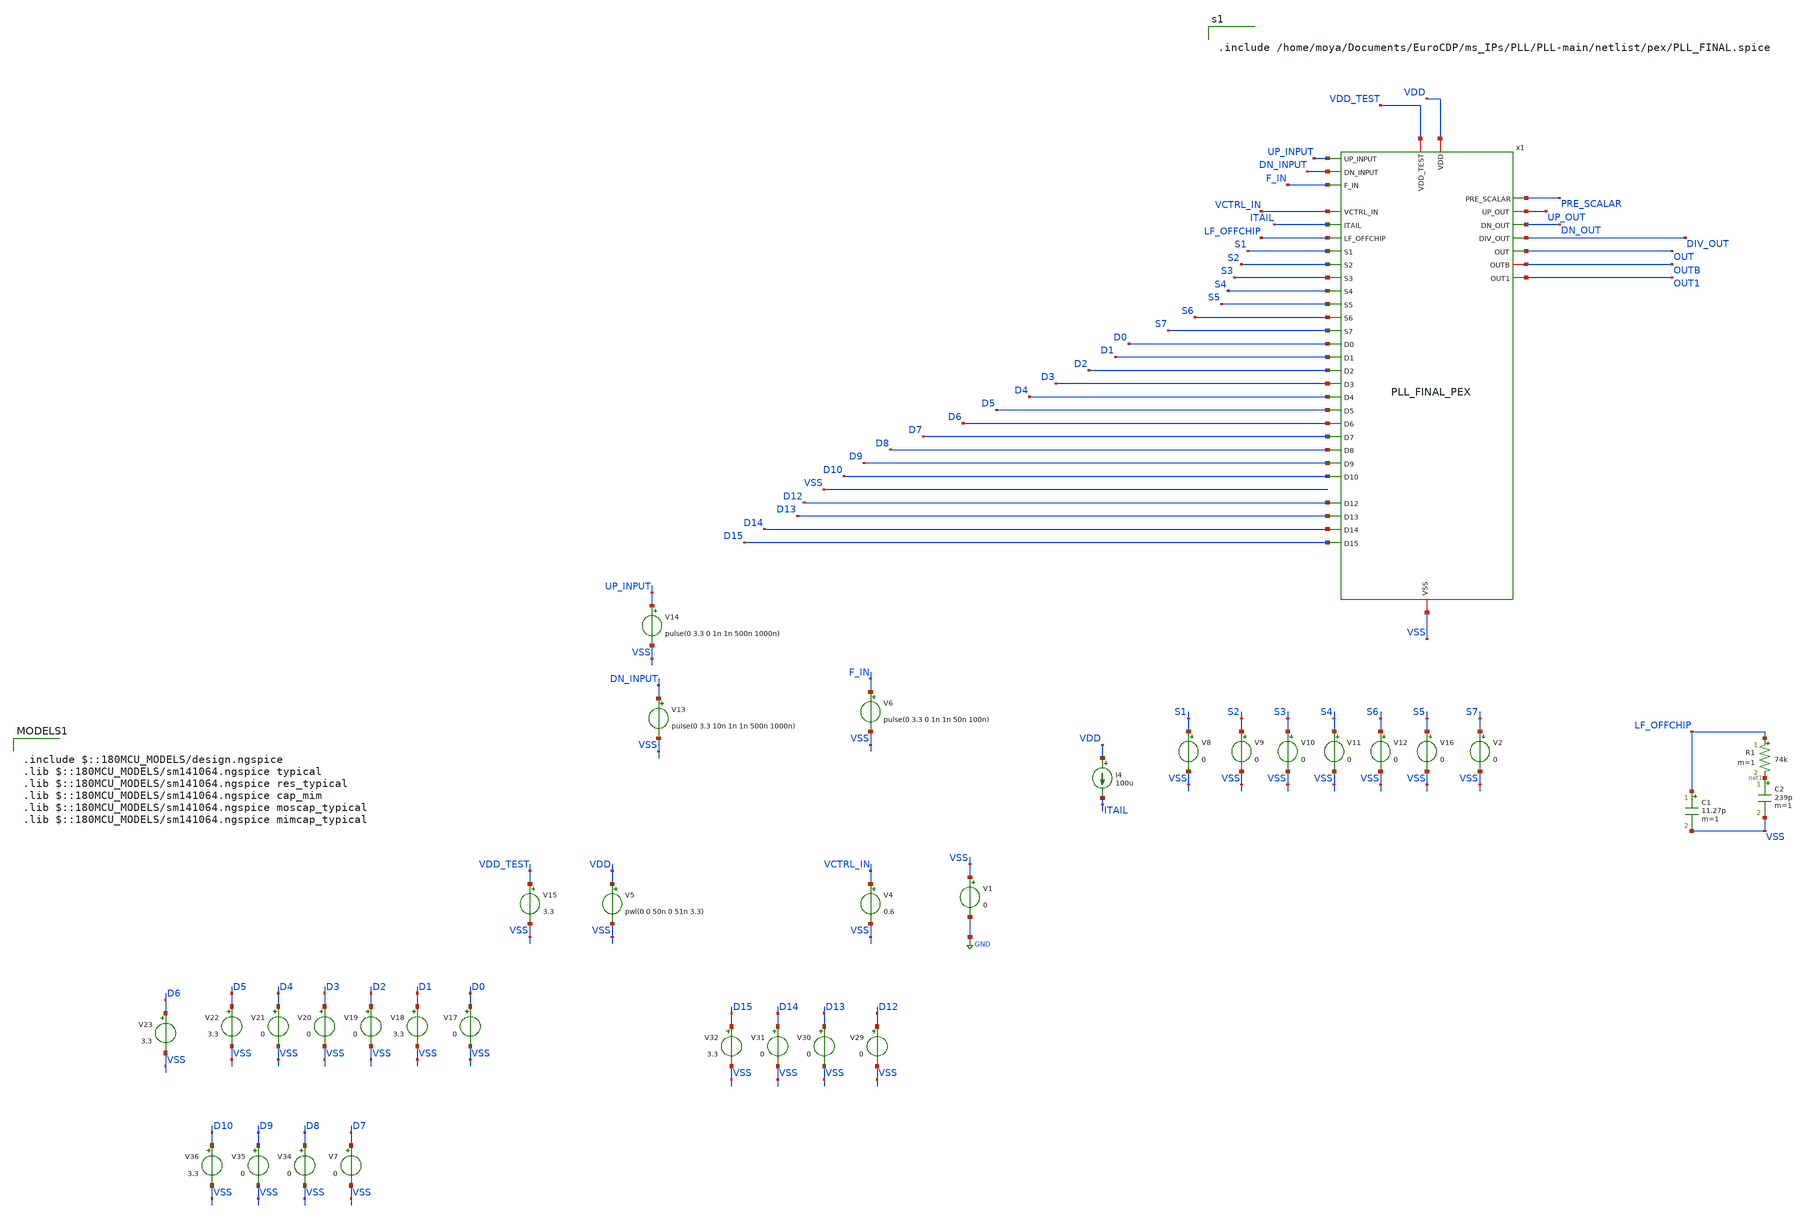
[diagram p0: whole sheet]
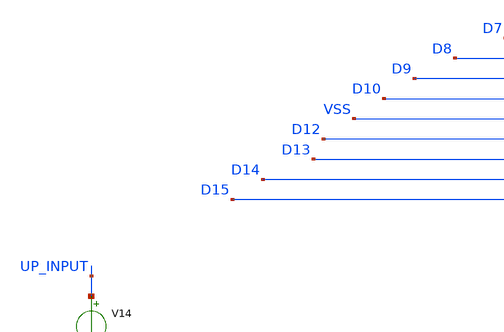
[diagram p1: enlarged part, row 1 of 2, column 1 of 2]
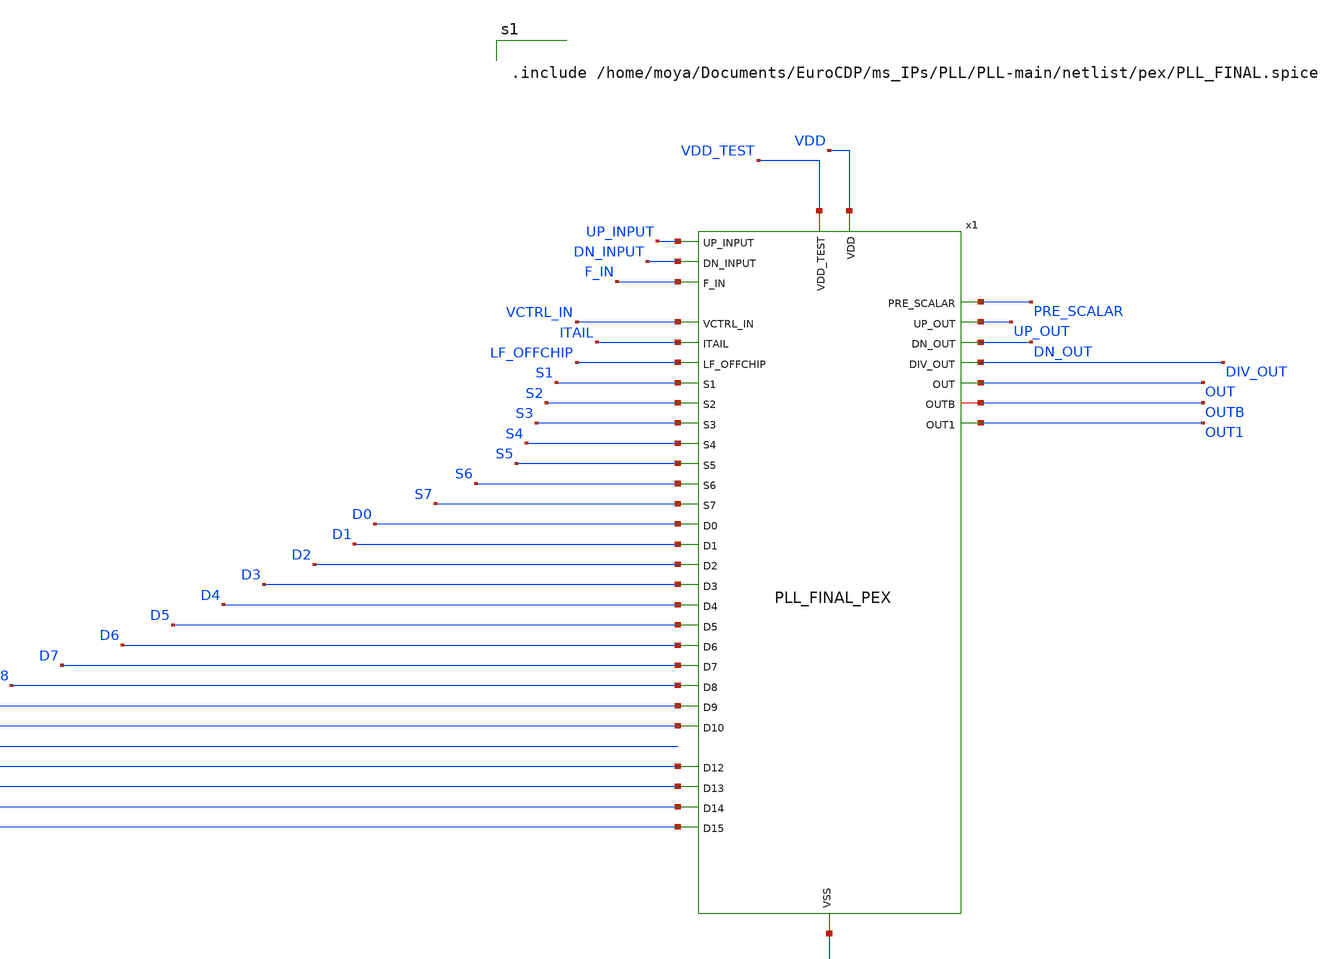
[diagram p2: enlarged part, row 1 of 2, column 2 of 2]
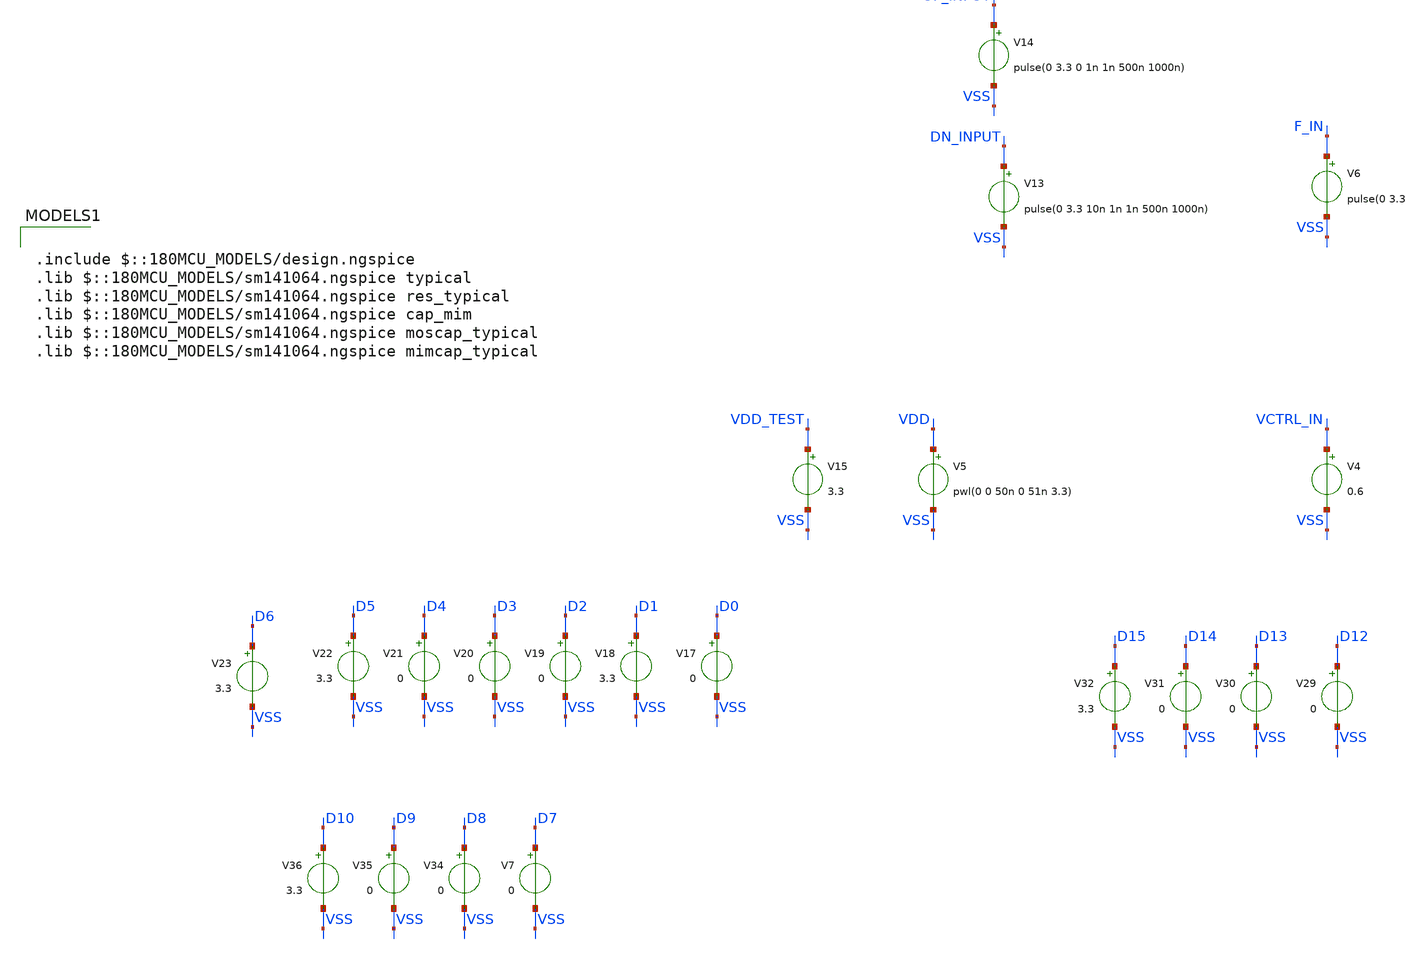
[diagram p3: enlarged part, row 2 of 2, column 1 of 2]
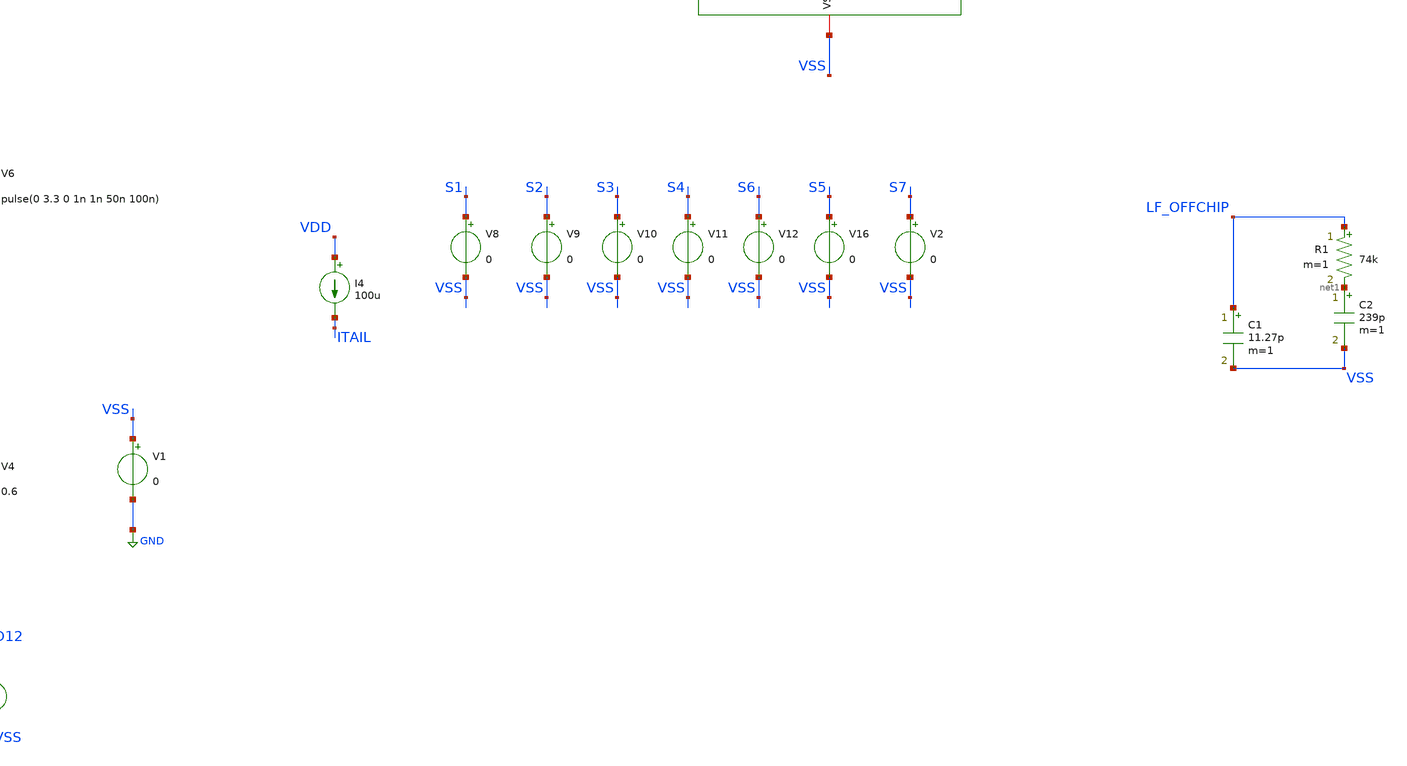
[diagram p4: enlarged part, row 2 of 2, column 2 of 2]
** sch_path: PLL-main/testbench/tran/xschem/TB_PLL_TOP_pex.sch
**.subckt TB_PLL_TOP_pex
V1 VSS GND 0
V4 VCTRL_IN VSS 0.6
V6 F_IN VSS pulse(0 3.3 0 1n 1n 50n 100n)
I4 VDD ITAIL 100u
V8 S1 VSS 0
V9 S2 VSS 0
V10 S3 VSS 0
V11 S4 VSS 0
V12 S6 VSS 0
V13 DN_INPUT VSS pulse(0 3.3 10n 1n 1n 500n 1000n)
V14 UP_INPUT VSS pulse(0 3.3 0 1n 1n 500n 1000n)
V15 VDD_TEST VSS 3.3
C1 LF_OFFCHIP VSS 11.27p m=1
R1 LF_OFFCHIP net1 74k m=1
C2 net1 VSS 239p m=1
V16 S5 VSS 0
V17 D0 VSS 0
V18 D1 VSS 3.3
V19 D2 VSS 0
V20 D3 VSS 0
V21 D4 VSS 0
V22 D5 VSS 3.3
V23 D6 VSS 3.3
V29 D12 VSS 0
V30 D13 VSS 0
V31 D14 VSS 0
V32 D15 VSS 3.3
V2 S7 VSS 0
V5 VDD VSS pwl(0 0 50n 0 51n 3.3)
V7 D7 VSS 0
V34 D8 VSS 0
V35 D9 VSS 0
V36 D10 VSS 3.3
x1 VDD_TEST D12 D0 UP_INPUT D13 D1 DN_INPUT VSS D14 D2 PRE_SCALAR UP_OUT D15 D3 F_IN DN_OUT D4 ITAIL
+ DIV_OUT D5 S1 S6 D6 VCTRL_IN D7 S2 D8 S3 OUT D9 OUTB S4 LF_OFFCHIP D10 S5 S7 OUT1 VDD PLL_FINAL
**** begin user architecture code


*.include pex_A_MUX.spice
*.include pex_VCO_DFF_C.spice
*.include Tappered-Buffer_1_pex.spice
*.include pex_PFD_T2.spice
*.include pex_CP.spice
*.include Res_74k_pex.spice
*.include pex_cap_11p.spice
*.include pex_cap_240p.spice
*.include pex_PLL_TOP_MUX_8.spice
*.include pex_7b_divider_magic.spice
*.include pex_PLL_TOP_MUX_2.spice
*.include Tappered-Buffer_1_pex.spice
*.option RSHUNT=1e18
**.option ABSTOL=1e-12
**.option VNTOL=1e-12
**.option CHGTOL=1e-14
.option RELTOL=1e-3
.option gmin=1e-12
**.option trtol=1
**.OPTION ITL4=500
.control
*save x1.vco_dff_c_0.vctrl.t19
*+ x1.pre_scalar.n0
*+ pre_scalar
*+ x1.vss.t6260
*+ x1.vdd.n7823
*+ x1.vctrl_in.t6
*+ x1.vctrl2.t62
*+ x1.vco_dff_c_0.vco_c_0.outb.t53
*+ x1.vco_dff_c_0.vco_c_0.inv_2_5.in.n34
*+ x1.vco_dff_c_0.vco_c_0.inv_2_3.out.n2
*+ x1.vco_dff_c_0.vco_c_0.inv_2_2.in.n30
*+ x1.vco_dff_c_0.vco_c_0.inv_2_0.in.n51
*++ x1.vco_dff_c_0.outb.t31
*+ x1.vco_dff_c_0.out.t10
*+ x1.up_out.t60
*+ x1.up_input.n12
*+ x1.up1.n10
*+ x1.up.n28
*+ x1.dn
*+ x1.a_mux_6.in1.n194
*+ x1.a_mux_5.in1.t163
*+ x1.a_mux_2.out.n14
*+ x1.a_mux_1.out
*+ x1.a_mux_6.out
*+ x1.7b_divider_magic_2.p2_gen_magic_0.dff_magic_0.tg_magic_3.out
*+ x1.7b_divider_magic_2.p2_gen_magic_0.dff_magic_0.tg_magic_3.clk
*+ x1.7b_divider_magic_2.p2_gen_magic_0.dff_magic_0.tg_magic_2.in.n10
*+ x1.7b_divider_magic_2.p2.t16
*+ x1.7b_divider_magic_2.out1.t8
*+ x1.7b_divider_magic_2.divide_by_2_1.tg_magic_3.out
*+ x1.7b_divider_magic_2.divide_by_2_1.tg_magic_3.clk
*+ x1.7b_divider_magic_1.p2_gen_magic_0.dff_magic_0.tg_magic_1.in.n19
*+ x1.7b_divider_magic_1.ld
*+ x1.7b_divider_magic_1.divide_by_2_1.tg_magic_2.in.n14
*+ x1.7b_divider_magic_1.divide_by_2_0.tg_magic_3.out
*+ x1.7b_divider_magic_1.divide_by_2_0.tg_magic_3.in
*+ x1.7b_divider_magic_0.out1
*+ x1.7b_divider_magic_0.ld.n38
*+ x1.vctrl_obv
*+ x1.a_mux_6.out.n27
*+ out1
save out
save outb
*+ net1
save lf_offchip
*+ itail1
*+ itail
save f_in
save dn_out
save up_out
*+ dn_input
save div_out
*set ngbehavior=hsa
*set ng_nomodcheck
tran 10n 100m
plot f_in+24 dn_out+20 up_out+16 lf_offchip+12 div_out+8 out+4 outb
write TB_PLL_TOP_pex.raw
.endc



.include $::180MCU_MODELS/design.ngspice
.lib $::180MCU_MODELS/sm141064.ngspice typical
.lib $::180MCU_MODELS/sm141064.ngspice res_typical
.lib $::180MCU_MODELS/sm141064.ngspice cap_mim
.lib $::180MCU_MODELS/sm141064.ngspice moscap_typical
.lib $::180MCU_MODELS/sm141064.ngspice mimcap_typical



.include /home/moya/Documents/EuroCDP/ms_IPs/PLL/PLL-main/netlist/pex/PLL_FINAL.spice


**** end user architecture code
**.ends
.GLOBAL GND
.end
